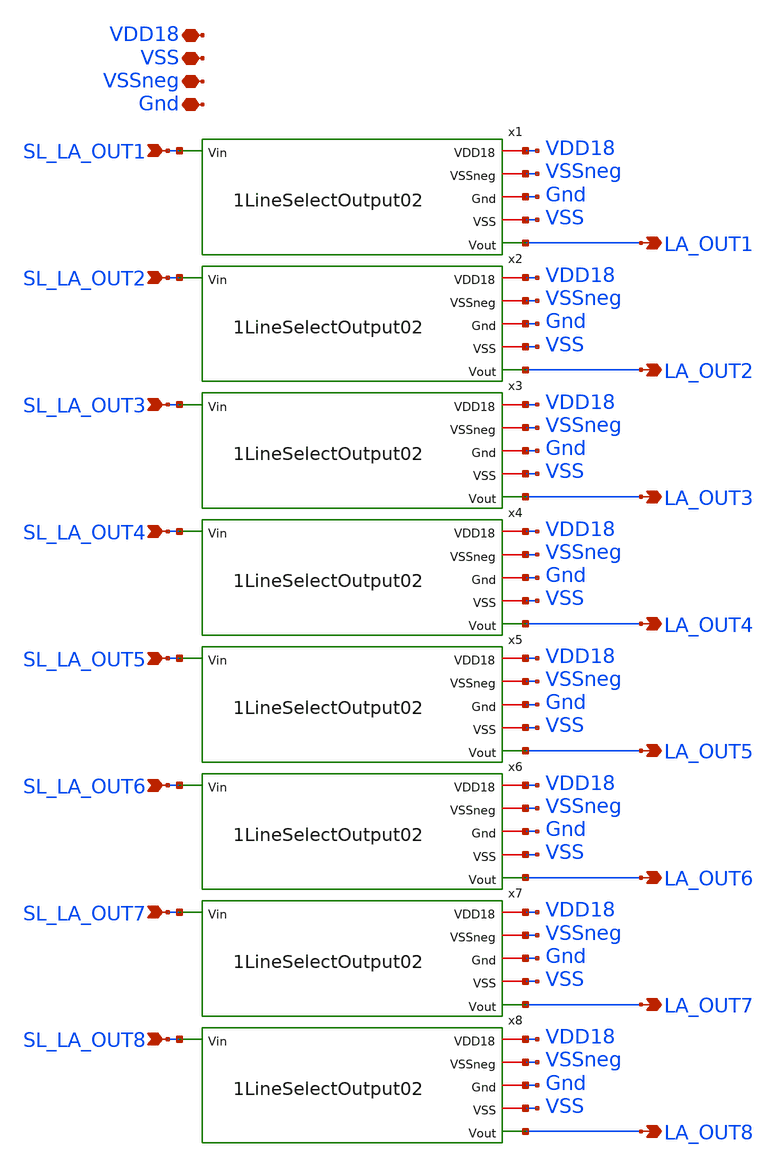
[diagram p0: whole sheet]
** sch_path: xschem/8LineSelectOutput02.sch
**.subckt 8LineSelectOutput02 SL_LA_OUT1 SL_LA_OUT2 SL_LA_OUT3 SL_LA_OUT4 SL_LA_OUT5 SL_LA_OUT6
*+ SL_LA_OUT7 SL_LA_OUT8 VDD18 VSS VSSneg LA_OUT1 LA_OUT2 LA_OUT3 LA_OUT4 LA_OUT5 LA_OUT6 LA_OUT7 LA_OUT8 Gnd
*.ipin SL_LA_OUT1
*.ipin SL_LA_OUT2
*.ipin SL_LA_OUT3
*.ipin SL_LA_OUT4
*.ipin SL_LA_OUT5
*.ipin SL_LA_OUT6
*.ipin SL_LA_OUT7
*.ipin SL_LA_OUT8
*.iopin VDD18
*.iopin VSS
*.iopin VSSneg
*.opin LA_OUT1
*.opin LA_OUT2
*.opin LA_OUT3
*.opin LA_OUT4
*.opin LA_OUT5
*.opin LA_OUT6
*.opin LA_OUT7
*.opin LA_OUT8
*.iopin Gnd
x1 VDD18 VSSneg Gnd VSS LA_OUT1 SL_LA_OUT1 1LineSelectOutput02
x2 VDD18 VSSneg Gnd VSS LA_OUT2 SL_LA_OUT2 1LineSelectOutput02
x3 VDD18 VSSneg Gnd VSS LA_OUT3 SL_LA_OUT3 1LineSelectOutput02
x4 VDD18 VSSneg Gnd VSS LA_OUT4 SL_LA_OUT4 1LineSelectOutput02
x5 VDD18 VSSneg Gnd VSS LA_OUT5 SL_LA_OUT5 1LineSelectOutput02
x6 VDD18 VSSneg Gnd VSS LA_OUT6 SL_LA_OUT6 1LineSelectOutput02
x7 VDD18 VSSneg Gnd VSS LA_OUT7 SL_LA_OUT7 1LineSelectOutput02
x8 VDD18 VSSneg Gnd VSS LA_OUT8 SL_LA_OUT8 1LineSelectOutput02
**.ends
.end
